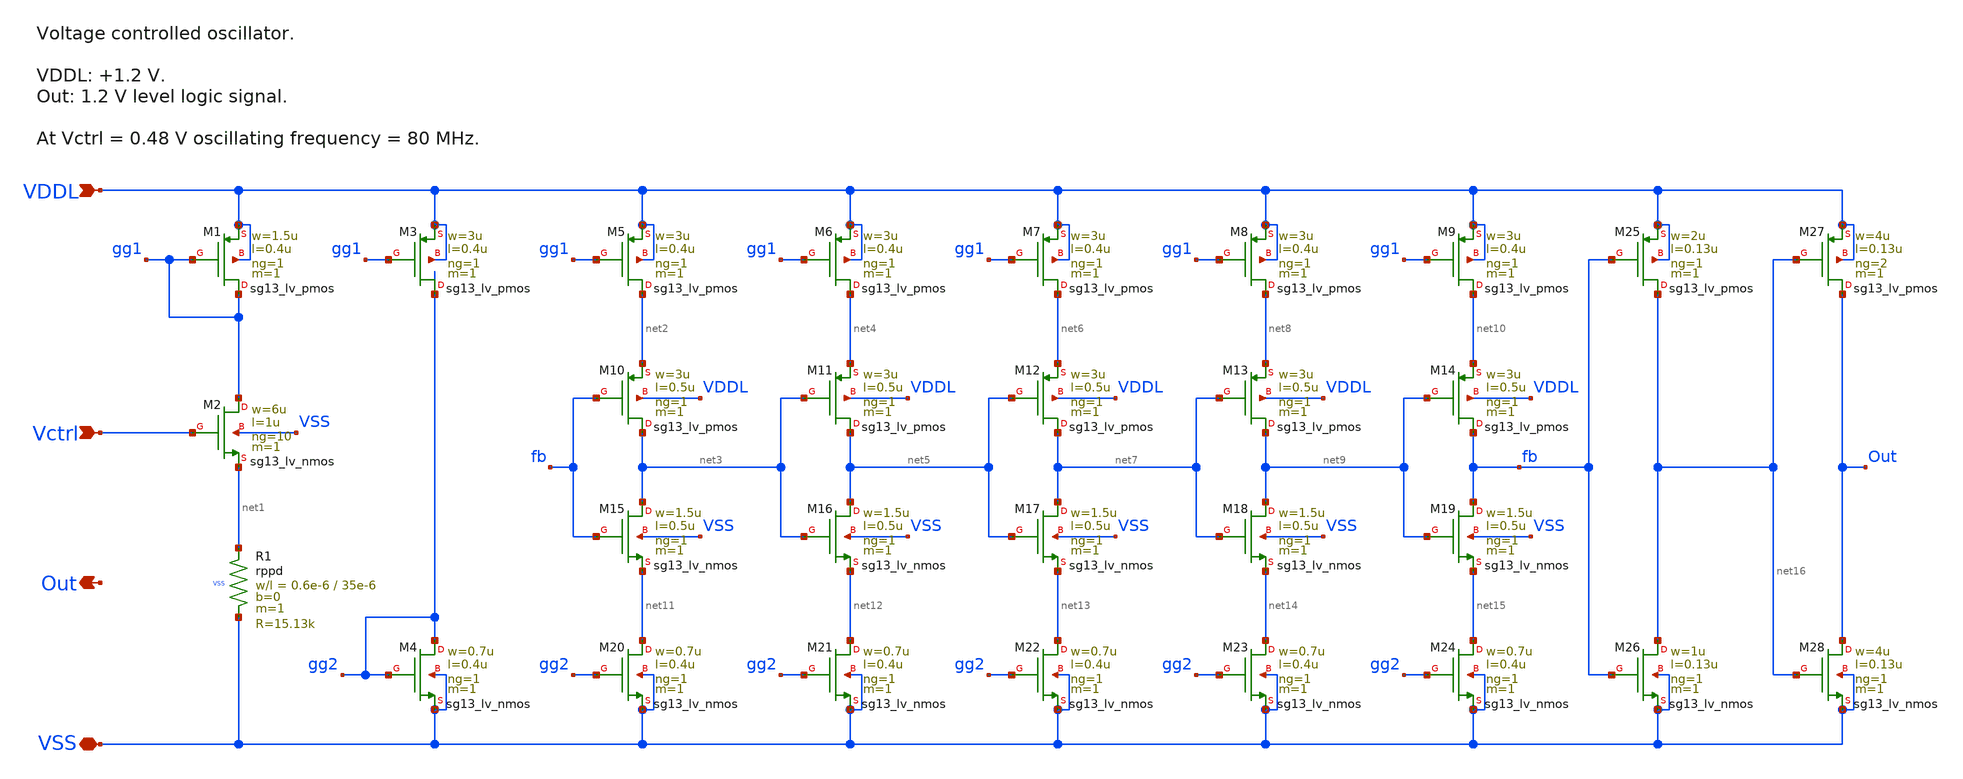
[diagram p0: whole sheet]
** sch_path: sar_adc/xschem/blocks/vco/vco.sch
**.subckt vco Vctrl VDDL VSS Out
*.ipin Vctrl
*.ipin VDDL
*.iopin VSS
*.opin Out
XM1 gg1 gg1 VDDL VDDL sg13_lv_pmos w=1.5u l=0.4u ng=1 m=1 mm_ok=1
XM3 gg2 gg1 VDDL VDDL sg13_lv_pmos w=3u l=0.4u ng=1 m=1 mm_ok=1
XR1 net1 VSS VSS rppd w=0.6e-6 l=35e-6 m=1 b=0 mm_ok=1
XM5 net2 gg1 VDDL VDDL sg13_lv_pmos w=3u l=0.4u ng=1 m=1 mm_ok=1
XM6 net4 gg1 VDDL VDDL sg13_lv_pmos w=3u l=0.4u ng=1 m=1 mm_ok=1
XM7 net6 gg1 VDDL VDDL sg13_lv_pmos w=3u l=0.4u ng=1 m=1 mm_ok=1
XM8 net8 gg1 VDDL VDDL sg13_lv_pmos w=3u l=0.4u ng=1 m=1 mm_ok=1
XM9 net10 gg1 VDDL VDDL sg13_lv_pmos w=3u l=0.4u ng=1 m=1 mm_ok=1
XM10 net3 fb net2 VDDL sg13_lv_pmos w=3u l=0.5u ng=1 m=1 mm_ok=1
XM11 net5 net3 net4 VDDL sg13_lv_pmos w=3u l=0.5u ng=1 m=1 mm_ok=1
XM12 net7 net5 net6 VDDL sg13_lv_pmos w=3u l=0.5u ng=1 m=1 mm_ok=1
XM13 net9 net7 net8 VDDL sg13_lv_pmos w=3u l=0.5u ng=1 m=1 mm_ok=1
XM14 fb net9 net10 VDDL sg13_lv_pmos w=3u l=0.5u ng=1 m=1 mm_ok=1
XM2 gg1 Vctrl net1 VSS sg13_lv_nmos w=6u l=1u ng=10 m=1 mm_ok=1
XM4 gg2 gg2 VSS VSS sg13_lv_nmos w=0.7u l=0.4u ng=1 m=1 mm_ok=1
XM15 net3 fb net11 VSS sg13_lv_nmos w=1.5u l=0.5u ng=1 m=1 mm_ok=1
XM16 net5 net3 net12 VSS sg13_lv_nmos w=1.5u l=0.5u ng=1 m=1 mm_ok=1
XM17 net7 net5 net13 VSS sg13_lv_nmos w=1.5u l=0.5u ng=1 m=1 mm_ok=1
XM18 net9 net7 net14 VSS sg13_lv_nmos w=1.5u l=0.5u ng=1 m=1 mm_ok=1
XM19 fb net9 net15 VSS sg13_lv_nmos w=1.5u l=0.5u ng=1 m=1 mm_ok=1
XM20 net11 gg2 VSS VSS sg13_lv_nmos w=0.7u l=0.4u ng=1 m=1 mm_ok=1
XM21 net12 gg2 VSS VSS sg13_lv_nmos w=0.7u l=0.4u ng=1 m=1 mm_ok=1
XM22 net13 gg2 VSS VSS sg13_lv_nmos w=0.7u l=0.4u ng=1 m=1 mm_ok=1
XM23 net14 gg2 VSS VSS sg13_lv_nmos w=0.7u l=0.4u ng=1 m=1 mm_ok=1
XM24 net15 gg2 VSS VSS sg13_lv_nmos w=0.7u l=0.4u ng=1 m=1 mm_ok=1
XM25 net16 fb VDDL VDDL sg13_lv_pmos w=2u l=0.13u ng=1 m=1 mm_ok=1
XM26 net16 fb VSS VSS sg13_lv_nmos w=1u l=0.13u ng=1 m=1 mm_ok=1
XM27 Out net16 VDDL VDDL sg13_lv_pmos w=4u l=0.13u ng=2 m=1 mm_ok=1
XM28 Out net16 VSS VSS sg13_lv_nmos w=4u l=0.13u ng=1 m=1 mm_ok=1
**.ends
.end
